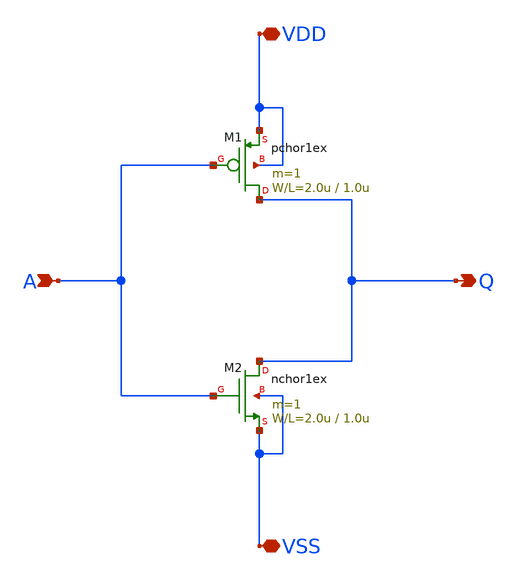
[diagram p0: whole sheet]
** sch_path: member_project/aiharayasuto/inverter.sch
**.subckt inverter Q A VDD VSS
*.opin Q
*.ipin A
*.iopin VDD
*.iopin VSS
M1 Q A VDD VDD pchor1ex L=1.0u W=2.0u m=1
M2 Q A VSS VSS nchor1ex L=1.0u W=2.0u m=1
**.ends
.end
